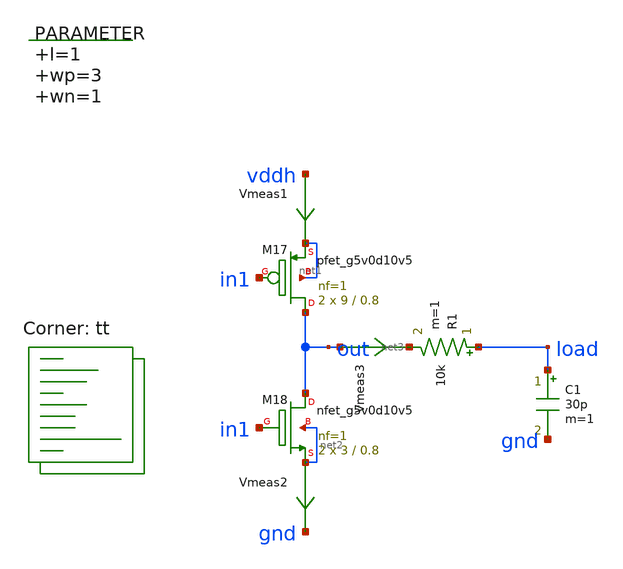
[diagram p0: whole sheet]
** sch_path: xschem/op_amp_output_stage_v2.sch
**.subckt op_amp_output_stage_v2
.param l=1 wp=3 wn=1
XM17 out in1 net1 net1 sky130_fd_pr__pfet_g5v0d10v5 L=0.8 W=9 nf=1 ad='int((nf+1)/2) * W/nf * 0.29' as='int((nf+2)/2) * W/nf * 0.29'
+ pd='2*int((nf+1)/2) * (W/nf + 0.29)' ps='2*int((nf+2)/2) * (W/nf + 0.29)' nrd='0.29 / W' nrs='0.29 / W'
+ sa=0 sb=0 sd=0 mult=2 m=2
XM18 out in1 net2 net2 sky130_fd_pr__nfet_g5v0d10v5 L=0.8 W=3 nf=1 ad='int((nf+1)/2) * W/nf * 0.29' as='int((nf+2)/2) * W/nf * 0.29'
+ pd='2*int((nf+1)/2) * (W/nf + 0.29)' ps='2*int((nf+2)/2) * (W/nf + 0.29)' nrd='0.29 / W' nrs='0.29 / W'
+ sa=0 sb=0 sd=0 mult=2 m=2
R1 load net3 10k m=1
C1 load gnd 30p m=1
Vmeas1 vddh net1 0
.save i(vmeas1)
Vmeas2 net2 gnd 0
.save i(vmeas2)
Vmeas3 out net3 0
.save i(vmeas3)
**** begin user architecture code
.lib $::SKYWATER_MODELS/sky130.lib.spice tt



  .option wnflag=1
  .option safecurrents
  ********************Static Current Sources***************************
  *Ivp vp gnd 5u
  *Ivn vddh vn 5u
  *Iip vddh ip 1u
  *Iin in gnd 1u
  ********************Static Voltage Sources***************************
  Vddh vddh gnd dc 5.5

  *vb1 vb1 gnd dc 3.37
  *vb2 vb2 gnd dc 1.95
  ********************Dynamic Voltage Sources***************************
  *******Calculation**********
  .param base_f=100e3 base_t={1/base_f} base_th={base_t/2} base_d={base_th}
  .param d2_th ={base_th} d2_t={2*d2_th}
  .param d1_th ={4*d2_th} d1_t={d0_th}
  .param d0_th ={4*d1_th} d0_t={4*d0_th}

  .param d20_d ={0} d21_d={1*d2_th} d22_d={2*d2_th} d23_d={3*d2_th}
  .param d10_d ={0} d11_d={1*d1_th} d12_d={2*d1_th} d13_d={3*d1_th}
  .param d00_d ={0} d01_d={1*d0_th} d02_d={2*d0_th} d03_d={3*d0_th}
  *******Signals**********
  .param vhi=5.5
*  Vin1 b[0] gnd pulse(0 {vhi} {0} 1p 1p {10u} {20u})
*  Vin2 b[1] gnd pulse(0 {vhi} {0} 1p 1p {20u} {40u})
  vin1 inx gnd sin({5.5/2} {5.5/2} 100k)
*  vin2 iny gnd sin({5.5/2} {-5.5/2} 100k)
  vin in1 gnd pulse({vhi} 0 {base_d} 1n 1n {base_th} {base_t})
  ********************Simulation Commands*****************************
  .control
     reset
     save all
     *dc vin 0 5.5 0.001
     *dc Iy 0 1u 0.001u
     tran 1n 50u
     *ac dec 100 1 10MEG
     write output_stage_v2-tb.raw
     set appendwrite
*    quit 0
  .endc



**** end user architecture code
**.ends
.end
